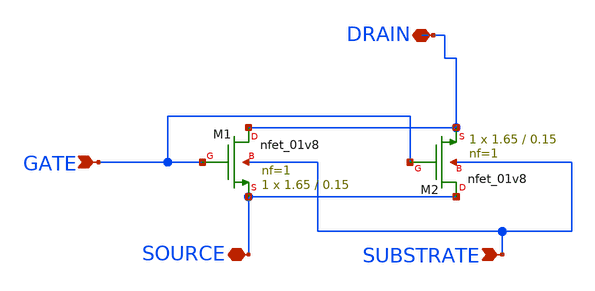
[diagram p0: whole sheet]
** sch_path: xschem/rf_nfet_01v8_aM02W1p65L0p15.sch
**.subckt rf_nfet_01v8_aM02W1p65L0p15 SOURCE DRAIN GATE SUBSTRATE
*.iopin SOURCE
*.iopin DRAIN
*.ipin GATE
*.ipin SUBSTRATE
XM1 DRAIN GATE SOURCE SUBSTRATE sky130_fd_pr__nfet_01v8 L=0.15 W=1.65 nf=1 ad='int((nf+1)/2) * W/nf * 0.29'
+ as='int((nf+2)/2) * W/nf * 0.29' pd='2*int((nf+1)/2) * (W/nf + 0.29)' ps='2*int((nf+2)/2) * (W/nf + 0.29)'
+ nrd='0.29 / W' nrs='0.29 / W' sa=0 sb=0 sd=0 mult=1 m=1
XM2 SOURCE GATE DRAIN SUBSTRATE sky130_fd_pr__nfet_01v8 L=0.15 W=1.65 nf=1 ad='int((nf+1)/2) * W/nf * 0.29'
+ as='int((nf+2)/2) * W/nf * 0.29' pd='2*int((nf+1)/2) * (W/nf + 0.29)' ps='2*int((nf+2)/2) * (W/nf + 0.29)'
+ nrd='0.29 / W' nrs='0.29 / W' sa=0 sb=0 sd=0 mult=1 m=1
**.ends
.end
